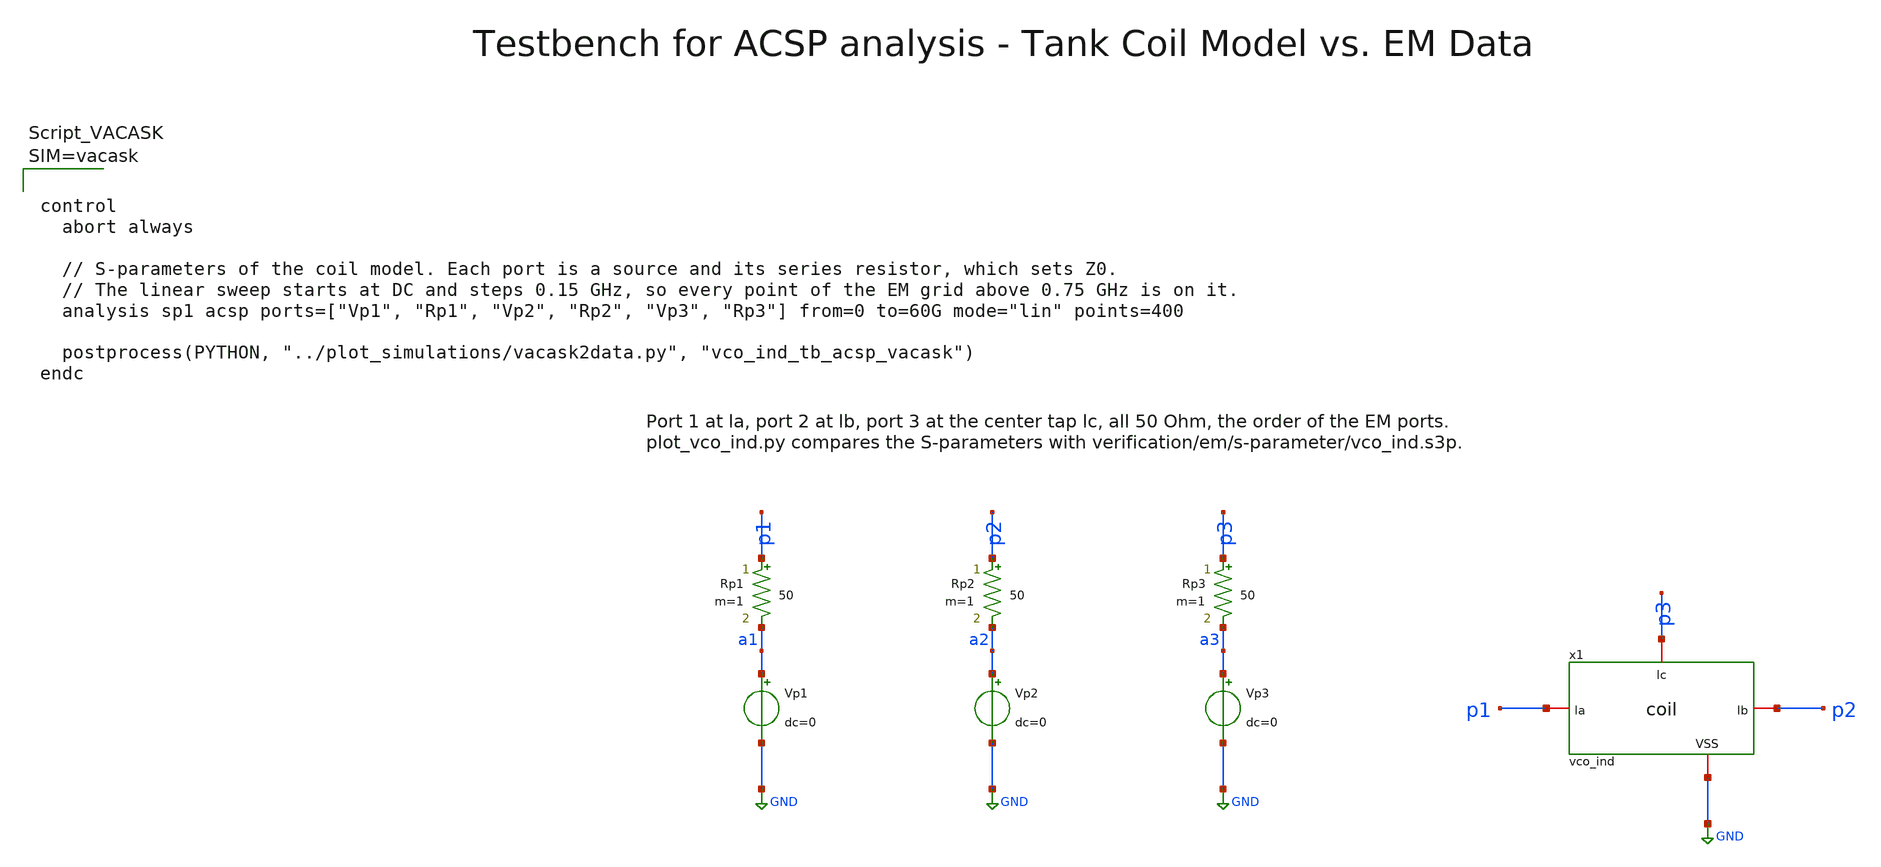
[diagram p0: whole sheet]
** sch_path: macros/vco/testbenches/xschem/vco_ind_tb_acsp_vacask.sch
**.subckt vco_ind_tb_acsp_vacask
x1 p1 p2 p3 GND vco_ind
Rp1 p1 a1 50 m=1
Vp1 a1 GND dc=0
Rp2 p2 a2 50 m=1
Vp2 a2 GND dc=0
Rp3 p3 a3 50 m=1
Vp3 a3 GND dc=0
**** begin user architecture code






**** end user architecture code
**.ends

* expanding   symbol:  vco_ind.sym # of pins=4
** sym_path: macros/vco/schematic/xschem/vco_ind.sym
** sch_path: macros/vco/schematic/xschem/vco_ind.sch
.subckt vco_ind la lb lc VSS
*.iopin la
*.iopin lc
*.iopin lb
*.iopin VSS
XL1 la lc lb VSS inductor3 w=4e-6 s=4e-6 d=52e-6 nr_r=2 m=1
x1 la lb lc vco_ind_le
.ends

.GLOBAL GND
.end
